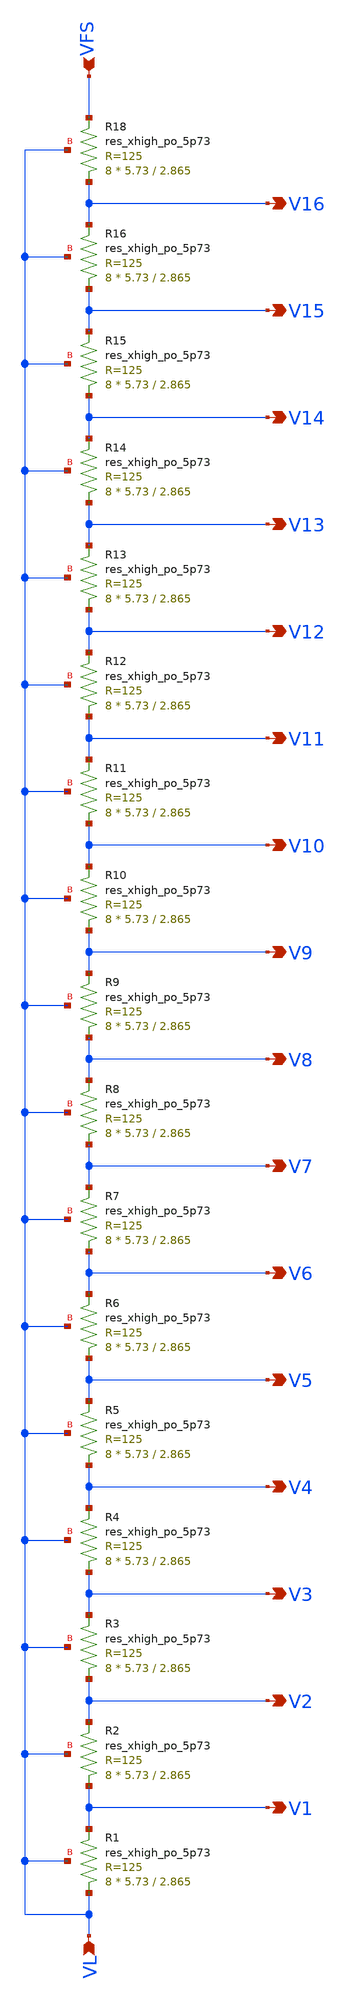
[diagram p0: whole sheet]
** sch_path: flashADC/xschem/resistorDivider_v0p0p1.sch
.lib $::SKYWATER_MODELS/sky130.lib.spice tt
.include $::SKYWATER_STDCELLS/sky130_fd_sc_hd.spice

**.subckt resistorDivider_v0p0p1 VFS VL V1 V2 V3 V4 V5 V6 V7 V8 V9 V10 V11 V12 V13 V14 V15 V16
*.ipin VFS
*.ipin VL
*.opin V1
*.opin V2
*.opin V3
*.opin V4
*.opin V5
*.opin V6
*.opin V7
*.opin V8
*.opin V9
*.opin V10
*.opin V11
*.opin V12
*.opin V13
*.opin V14
*.opin V15
*.opin V16
XR1 VL V1 VL sky130_fd_pr__res_xhigh_po_5p73 L=2.865 mult=8 m=8
XR2 V1 V2 VL sky130_fd_pr__res_xhigh_po_5p73 L=2.865 mult=8 m=8
XR3 V2 V3 VL sky130_fd_pr__res_xhigh_po_5p73 L=2.865 mult=8 m=8
XR4 V3 V4 VL sky130_fd_pr__res_xhigh_po_5p73 L=2.865 mult=8 m=8
XR5 V4 V5 VL sky130_fd_pr__res_xhigh_po_5p73 L=2.865 mult=8 m=8
XR6 V5 V6 VL sky130_fd_pr__res_xhigh_po_5p73 L=2.865 mult=8 m=8
XR7 V6 V7 VL sky130_fd_pr__res_xhigh_po_5p73 L=2.865 mult=8 m=8
XR8 V7 V8 VL sky130_fd_pr__res_xhigh_po_5p73 L=2.865 mult=8 m=8
XR9 V8 V9 VL sky130_fd_pr__res_xhigh_po_5p73 L=2.865 mult=8 m=8
XR10 V9 V10 VL sky130_fd_pr__res_xhigh_po_5p73 L=2.865 mult=8 m=8
XR11 V10 V11 VL sky130_fd_pr__res_xhigh_po_5p73 L=2.865 mult=8 m=8
XR12 V11 V12 VL sky130_fd_pr__res_xhigh_po_5p73 L=2.865 mult=8 m=8
XR13 V12 V13 VL sky130_fd_pr__res_xhigh_po_5p73 L=2.865 mult=8 m=8
XR14 V13 V14 VL sky130_fd_pr__res_xhigh_po_5p73 L=2.865 mult=8 m=8
XR15 V14 V15 VL sky130_fd_pr__res_xhigh_po_5p73 L=2.865 mult=8 m=8
XR16 V15 V16 VL sky130_fd_pr__res_xhigh_po_5p73 L=2.865 mult=8 m=8
XR18 V16 VFS VL sky130_fd_pr__res_xhigh_po_5p73 L=2.865 mult=8 m=8
**.ends
.end
